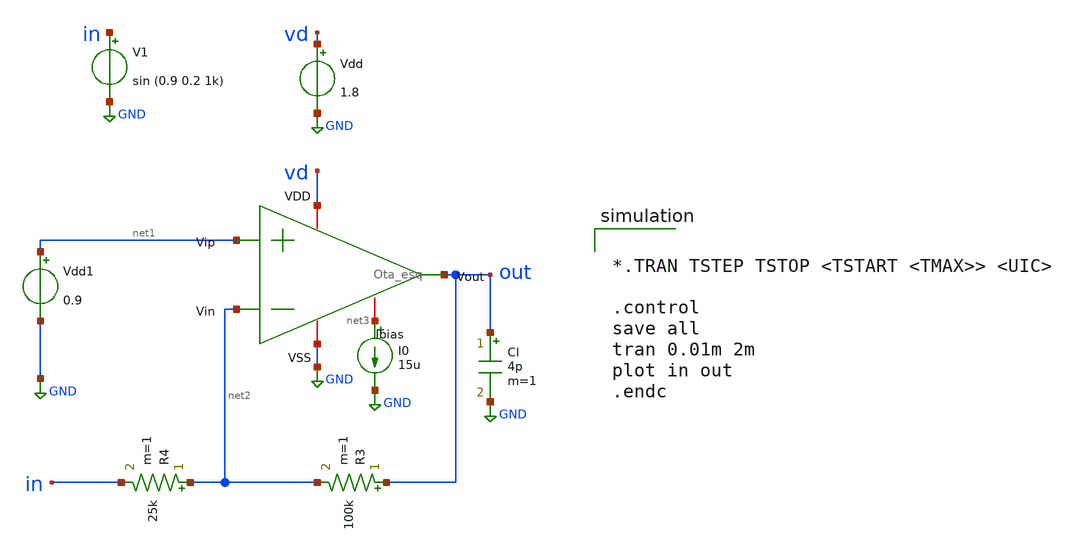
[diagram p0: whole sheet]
** sch_path: xschem/ota_feedbacb_tb.sch
**.subckt ota_feedbacb_tb
Vdd vd GND 1.8
I0 net3 GND 15u
V1 in GND sin (0.9 0.2 1k)
Cl out GND 4p m=1
x1 vd net2 net1 out net3 GND Ota_esq
R3 out net2 100k m=1
R4 net2 in 25k m=1
Vdd1 net1 GND 0.9
**** begin user architecture code

** opencircuitdesign pdks install
.lib $::SKYWATER_MODELS/sky130.lib.spice tt




*.TRAN TSTEP TSTOP <TSTART <TMAX>> <UIC>

.control
save all
tran 0.01m 2m
plot in out
.endc


**** end user architecture code
**.ends

* expanding   symbol:  Ota_esq.sym # of pins=6
** sym_path: Ota_esq.sym
** sch_path: Ota_esq.sch
.subckt Ota_esq VDD Vin Vip Vout Ibias VSS
*.ipin Vin
*.ipin Vip
*.iopin VDD
*.iopin VSS
*.iopin Ibias
*.opin Vout
XM1 net1 Vin net3 net3 sky130_fd_pr__pfet_01v8 L=1 W=1 nf=1 ad='int((nf+1)/2) * W/nf * 0.29' as='int((nf+2)/2) * W/nf * 0.29'
+ pd='2*int((nf+1)/2) * (W/nf + 0.29)' ps='2*int((nf+2)/2) * (W/nf + 0.29)' nrd='0.29 / W' nrs='0.29 / W'
+ sa=0 sb=0 sd=0 mult=1 m=1
XM2 net2 Vip net3 net3 sky130_fd_pr__pfet_01v8 L=1 W=1 nf=1 ad='int((nf+1)/2) * W/nf * 0.29' as='int((nf+2)/2) * W/nf * 0.29'
+ pd='2*int((nf+1)/2) * (W/nf + 0.29)' ps='2*int((nf+2)/2) * (W/nf + 0.29)' nrd='0.29 / W' nrs='0.29 / W'
+ sa=0 sb=0 sd=0 mult=1 m=1
XM3 net1 net1 VSS VSS sky130_fd_pr__nfet_01v8 L=8 W=0.5 nf=1 ad='int((nf+1)/2) * W/nf * 0.29' as='int((nf+2)/2) * W/nf * 0.29'
+ pd='2*int((nf+1)/2) * (W/nf + 0.29)' ps='2*int((nf+2)/2) * (W/nf + 0.29)' nrd='0.29 / W' nrs='0.29 / W'
+ sa=0 sb=0 sd=0 mult=1 m=1
XM4 net2 net1 VSS VSS sky130_fd_pr__nfet_01v8 L=8 W=0.5 nf=1 ad='int((nf+1)/2) * W/nf * 0.29' as='int((nf+2)/2) * W/nf * 0.29'
+ pd='2*int((nf+1)/2) * (W/nf + 0.29)' ps='2*int((nf+2)/2) * (W/nf + 0.29)' nrd='0.29 / W' nrs='0.29 / W'
+ sa=0 sb=0 sd=0 mult=1 m=1
XM5 net3 Ibias VDD VDD sky130_fd_pr__pfet_01v8 L=1 W=24 nf=8 ad='int((nf+1)/2) * W/nf * 0.29' as='int((nf+2)/2) * W/nf * 0.29'
+ pd='2*int((nf+1)/2) * (W/nf + 0.29)' ps='2*int((nf+2)/2) * (W/nf + 0.29)' nrd='0.29 / W' nrs='0.29 / W'
+ sa=0 sb=0 sd=0 mult=1 m=1
XM8 Ibias Ibias VDD VDD sky130_fd_pr__pfet_01v8 L=1 W=24 nf=8 ad='int((nf+1)/2) * W/nf * 0.29' as='int((nf+2)/2) * W/nf * 0.29'
+ pd='2*int((nf+1)/2) * (W/nf + 0.29)' ps='2*int((nf+2)/2) * (W/nf + 0.29)' nrd='0.29 / W' nrs='0.29 / W'
+ sa=0 sb=0 sd=0 mult=1 m=1
XM6 Vout Ibias VDD VDD sky130_fd_pr__pfet_01v8 L=1 W=39 nf=13 ad='int((nf+1)/2) * W/nf * 0.29' as='int((nf+2)/2) * W/nf * 0.29'
+ pd='2*int((nf+1)/2) * (W/nf + 0.29)' ps='2*int((nf+2)/2) * (W/nf + 0.29)' nrd='0.29 / W' nrs='0.29 / W'
+ sa=0 sb=0 sd=0 mult=1 m=1
XM7 Vout net2 VSS VSS sky130_fd_pr__nfet_01v8 L=1 W=21 nf=7 ad='int((nf+1)/2) * W/nf * 0.29' as='int((nf+2)/2) * W/nf * 0.29'
+ pd='2*int((nf+1)/2) * (W/nf + 0.29)' ps='2*int((nf+2)/2) * (W/nf + 0.29)' nrd='0.29 / W' nrs='0.29 / W'
+ sa=0 sb=0 sd=0 mult=1 m=1
XC1 net2 Vout sky130_fd_pr__cap_mim_m3_1 W=23 L=23 MF=1 m=1
.ends

.GLOBAL GND
.end
